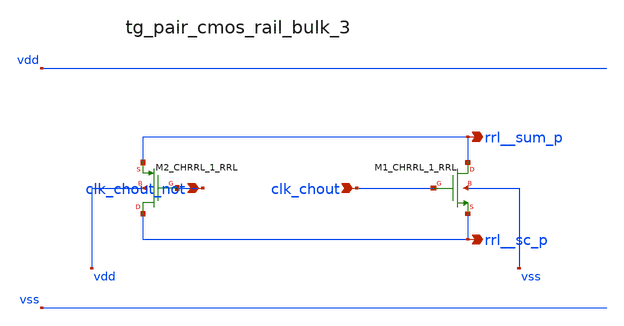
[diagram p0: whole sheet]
** sch_path: analog-db/raw/ia_004_fan_chopper_rrl/hier/blocks/tg_pair_cmos_rail_bulk_3.sch
**.subckt tg_pair_cmos_rail_bulk_3 clk_chout_not clk_chout rrl__sum_p rrl__sc_p
*.ipin clk_chout_not
*.ipin clk_chout
*.opin rrl__sum_p
*.opin rrl__sc_p
XM1_CHRRL_1_RRL rrl__sum_p clk_chout rrl__sc_p vss sg13_lv_nmos w=x_dut_xm1_chrrl_1_rrl_w
+ l=x_dut_xm1_chrrl_1_rrl_l ng=1 m=x_dut_xm1_chrrl_1_rrl_m
XM2_CHRRL_1_RRL rrl__sc_p clk_chout_not rrl__sum_p vdd sg13_lv_pmos w=x_dut_xm2_chrrl_1_rrl_w
+ l=x_dut_xm2_chrrl_1_rrl_l ng=1 m=x_dut_xm2_chrrl_1_rrl_m
**.ends
.end
